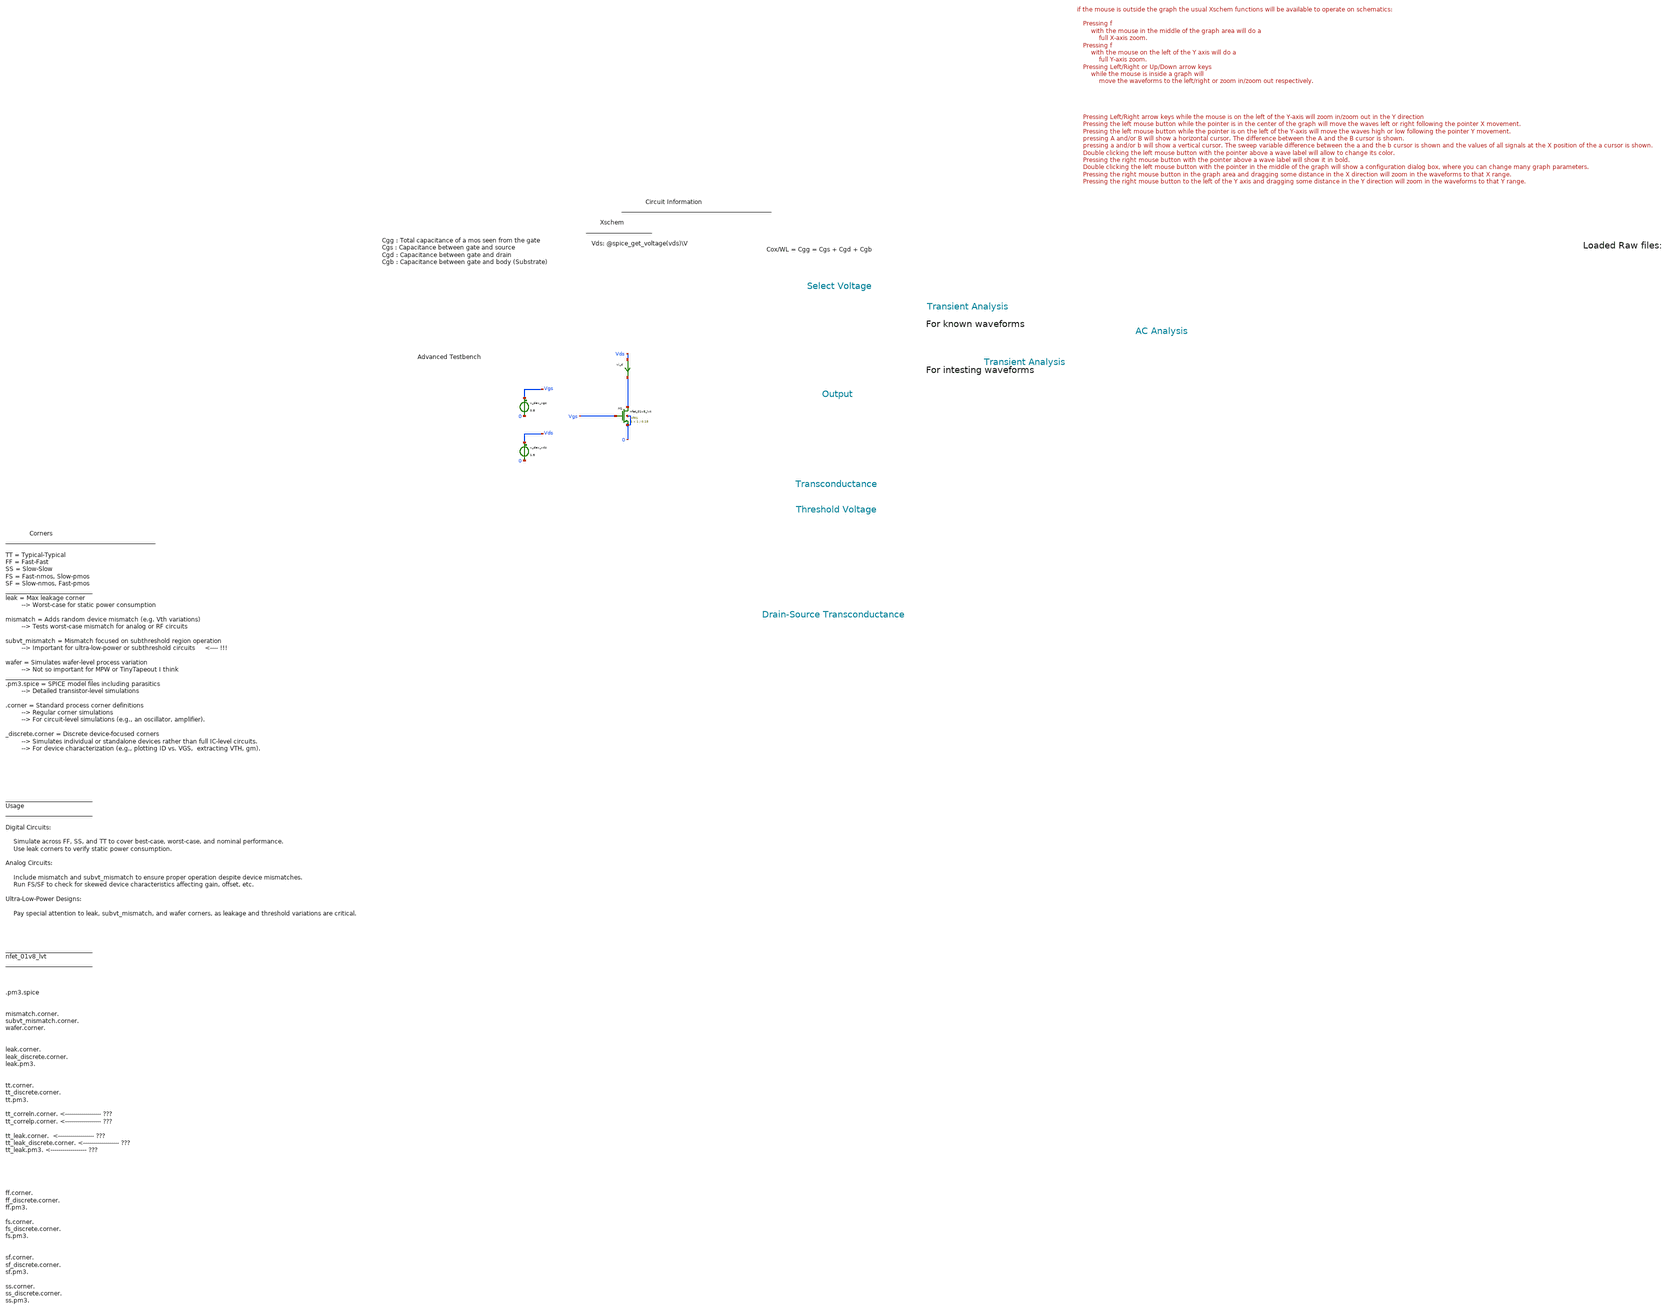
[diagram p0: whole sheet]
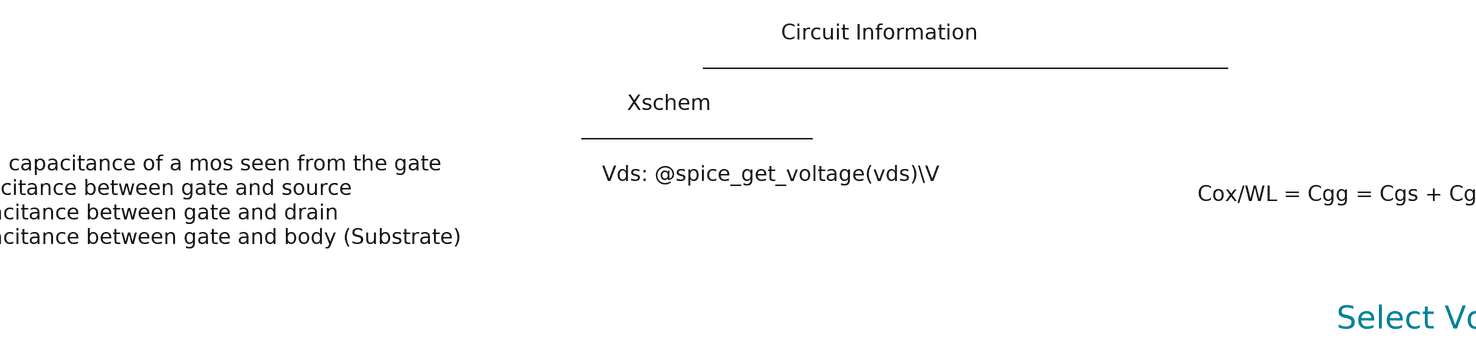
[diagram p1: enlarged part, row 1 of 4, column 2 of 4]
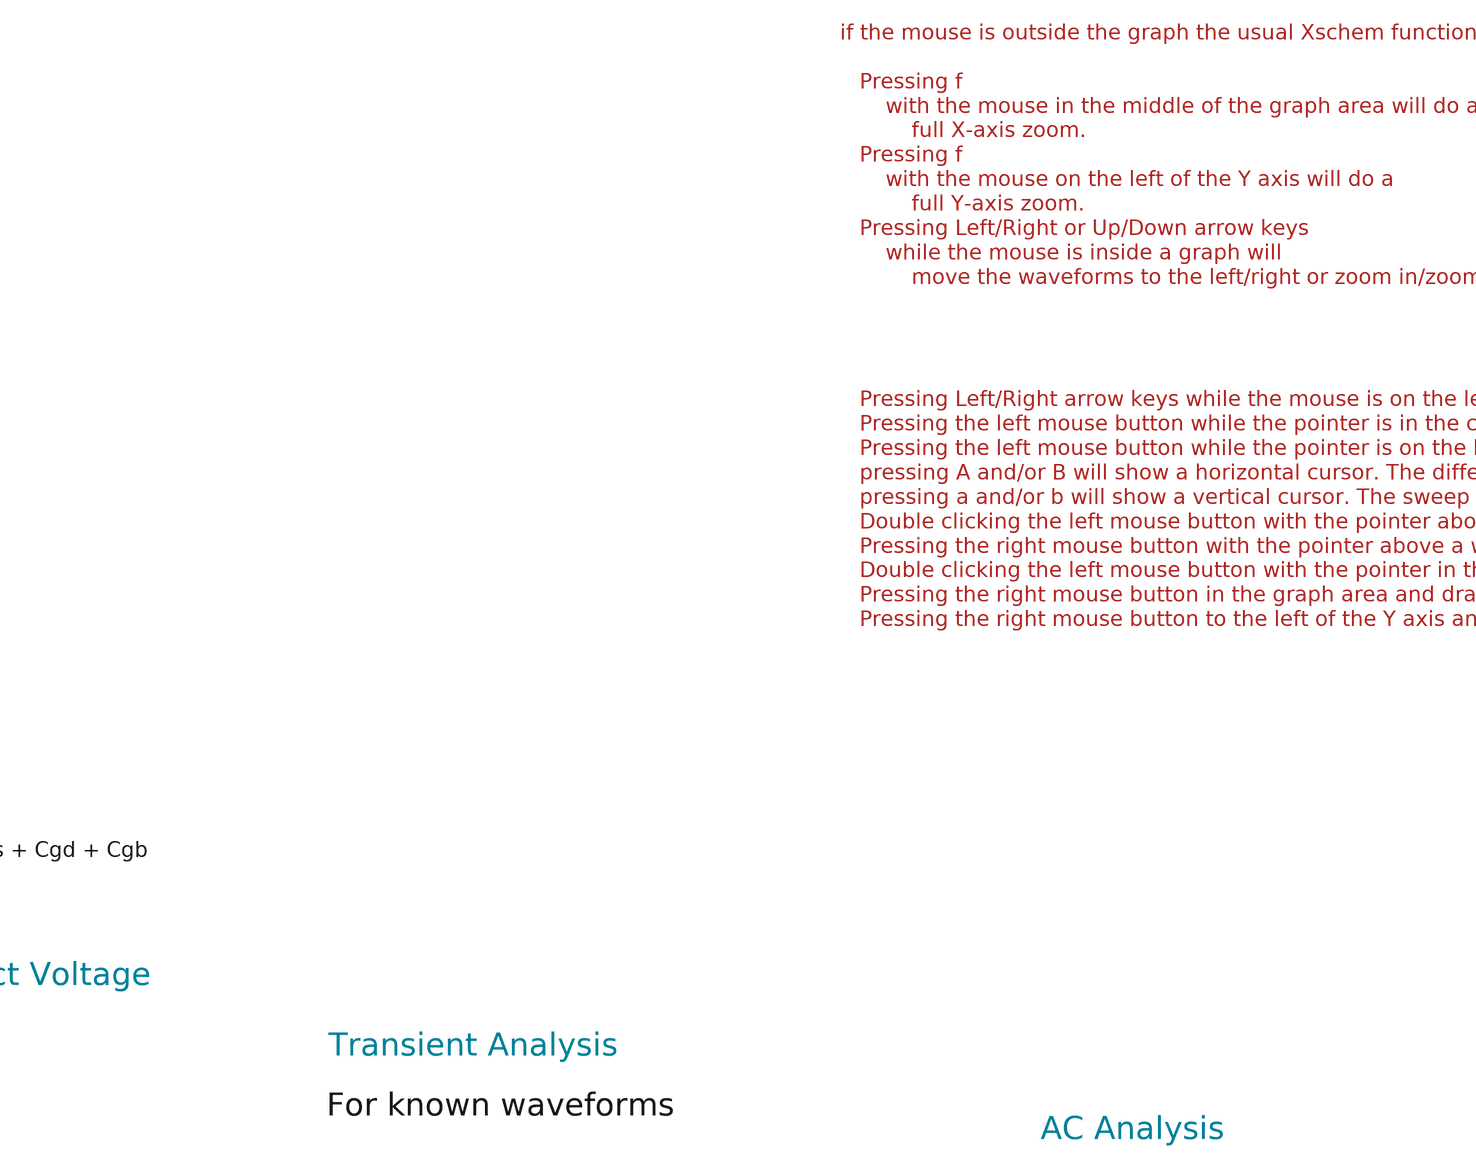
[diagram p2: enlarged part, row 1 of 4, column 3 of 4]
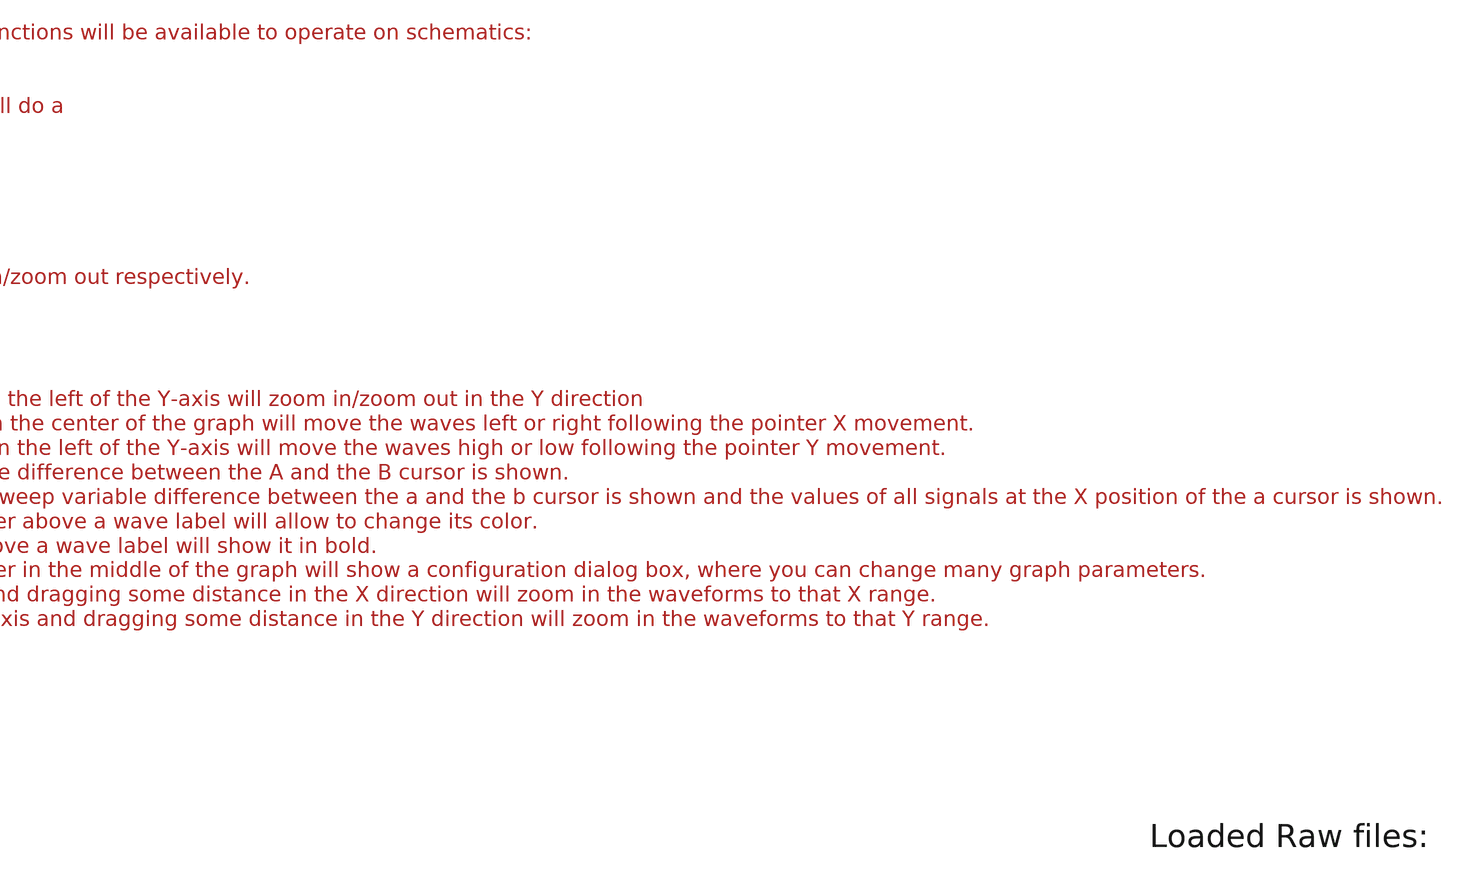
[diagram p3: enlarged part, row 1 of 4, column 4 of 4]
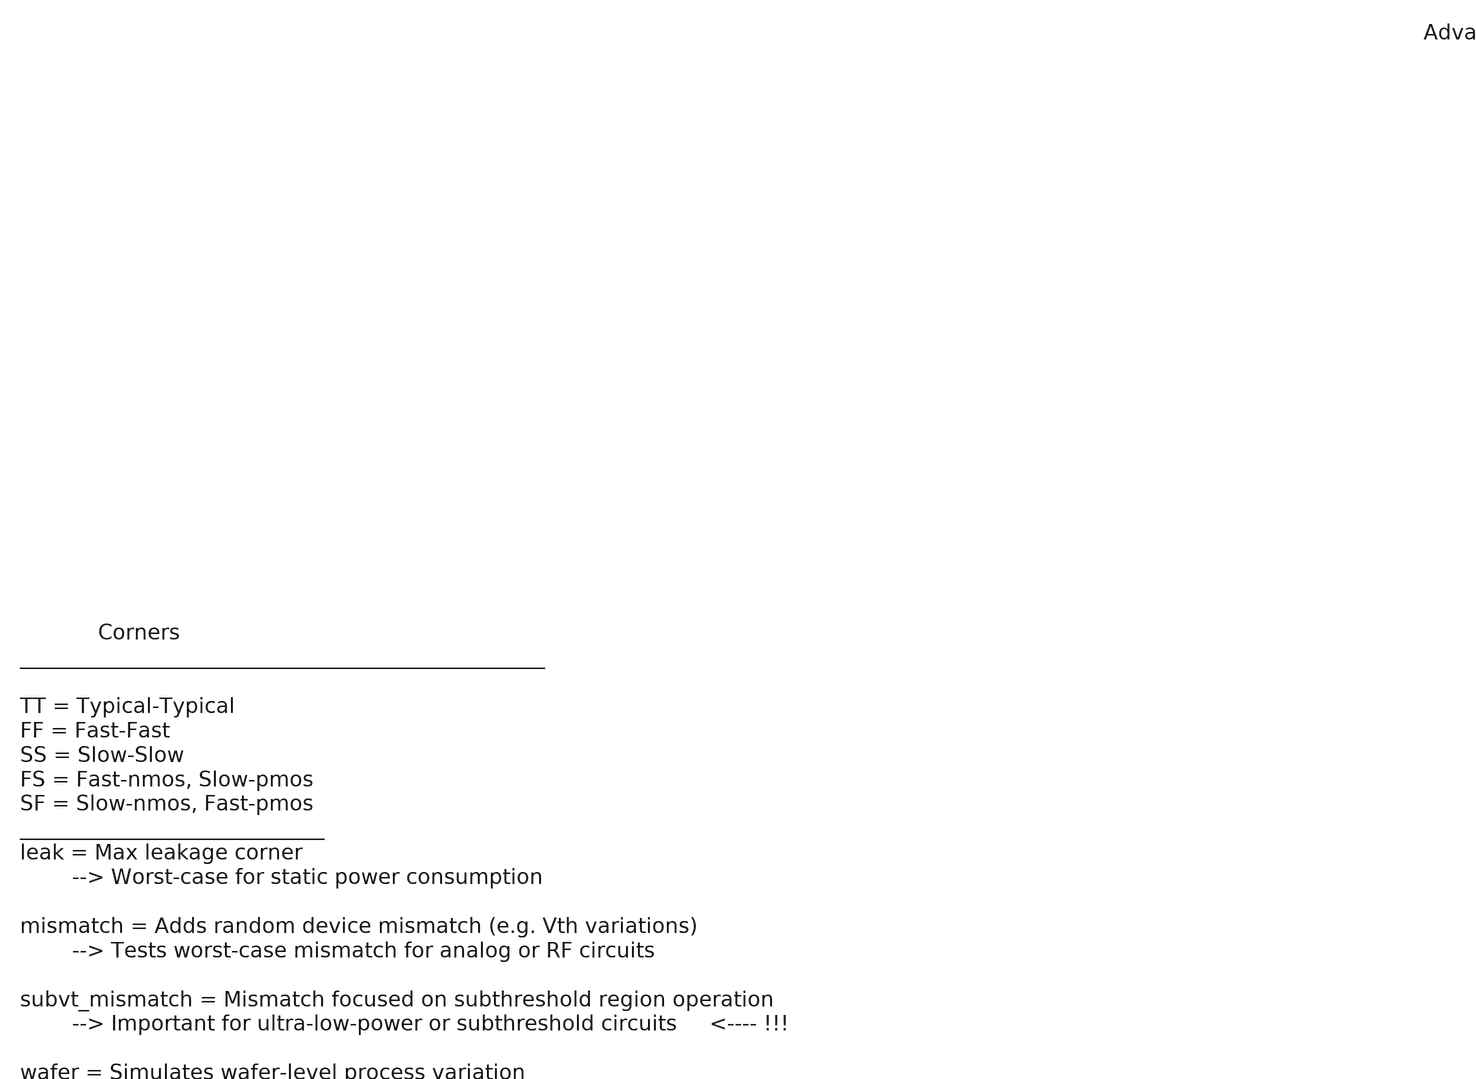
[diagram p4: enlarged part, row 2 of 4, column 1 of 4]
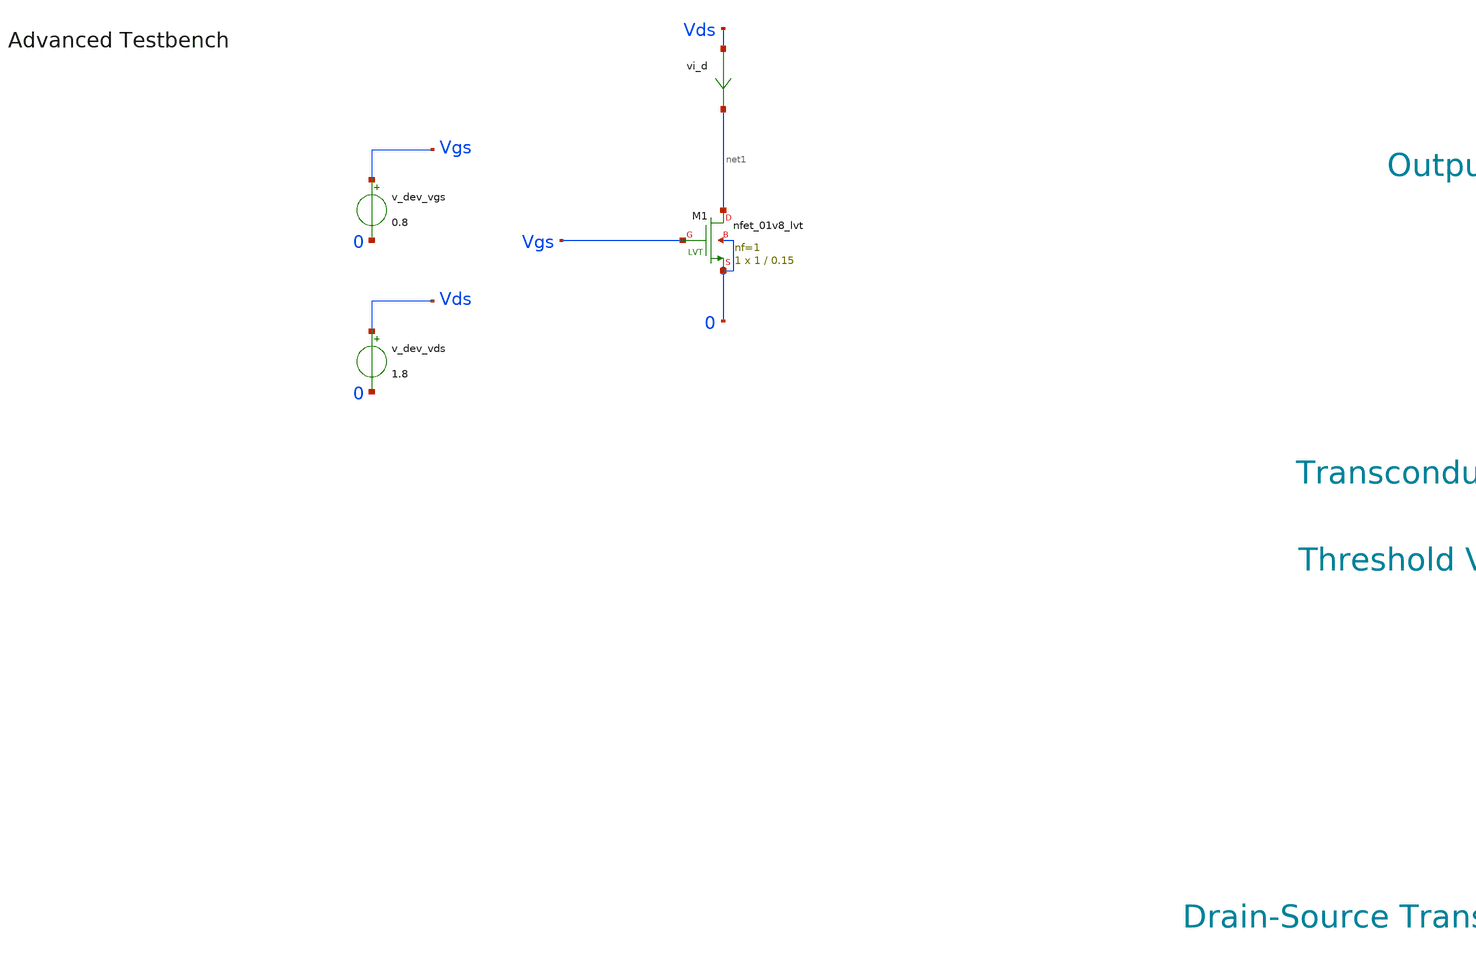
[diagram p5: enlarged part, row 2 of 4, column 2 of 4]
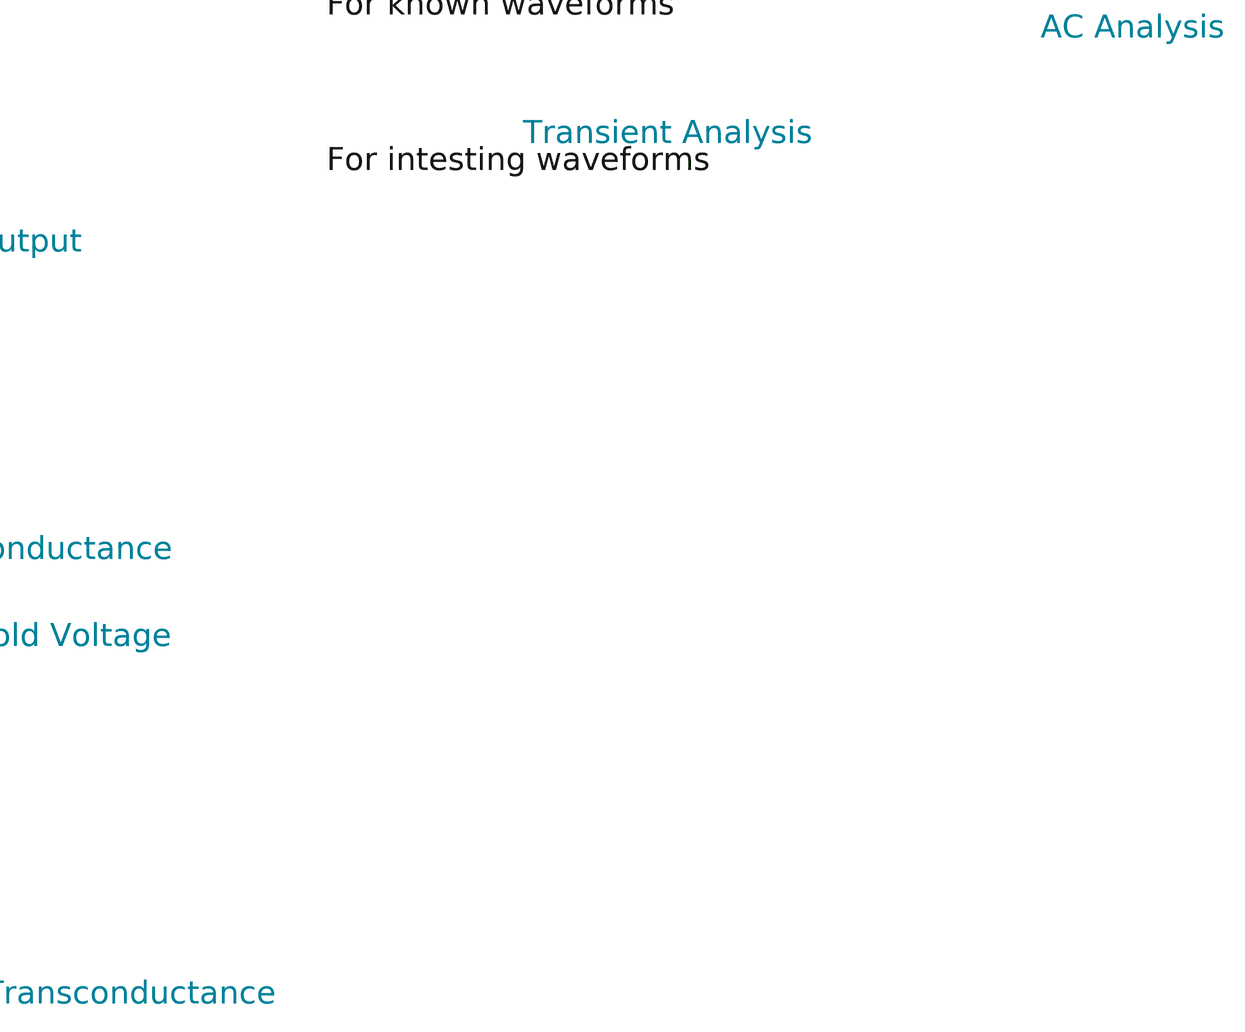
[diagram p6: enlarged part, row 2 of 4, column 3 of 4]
** sch_path: xschem/T0/nmos.sch
* Copyright (C) 1998-2024 Stefan Frederik Schippers
* This program is free software; you can redistribute it and/or modify
* it under the terms of the GNU General Public License as published by
* the Free Software Foundation; either version 2 of the License, or
* (at your option) any later version.
* This program is distributed in the hope that it will be useful,
* but WITHOUT ANY WARRANTY; without even the implied warranty of
* MERCHANTABILITY or FITNESS FOR A PARTICULAR PURPOSE.  See the
* GNU General Public License for more details.
* You should have received a copy of the GNU General Public License
* along with this program; if not, write to the Free Software
**.subckt nmos
XM1 net1 Vgs 0 0 sky130_fd_pr__nfet_01v8_lvt L=0.15 W=1 nf=1 ad='int((1 + 1)/2) * 1 / 1 * 0.29' as='int((1 + 2)/2) * 1 / 1 * 0.29'
+ pd='2*int((1 + 1)/2) * (1 / 1 + 0.29)' ps='2*int((1 + 2)/2) * (1 / 1 + 0.29)' nrd='0.29 / 1 ' nrs='0.29 / 1 '
+ sa=0 sb=0 sd=0 mult=1 m=1
vi_d Vds net1 0
.save i(vi_d)
v_dev_vds Vds 0 1.8
v_dev_vgs Vgs 0 0.8
**** begin user architecture code



.temp 30
*.param w_width = 1
*.param l_length = 0.15
*.option gmin=5n
*.option scale=1e-6
*.option wnflag=1
.option savecurrents

.save all
.control
  save all alli

  save @m.xm1.msky130_fd_pr__nfet_01v8_lvt[gm]
  save @m.xm1.msky130_fd_pr__nfet_01v8_lvt[id]
  save @m.xm1.msky130_fd_pr__nfet_01v8_lvt[vgs]

  save @m.xm1.msky130_fd_pr__nfet_01v8_lvt[cgg]
  save @m.xm1.msky130_fd_pr__nfet_01v8_lvt[cgs]
  save @m.xm1.msky130_fd_pr__nfet_01v8_lvt[cgd]
  save @m.xm1.msky130_fd_pr__nfet_01v8_lvt[cgb]

  save @m.xm1.msky130_fd_pr__nfet_01v8_lvt[vds]
  save @m.xm1.msky130_fd_pr__nfet_01v8_lvt[vdsat]
  save @m.xm1.msky130_fd_pr__nfet_01v8_lvt[vth]


  save @m.xm1.msky130_fd_pr__nfet_01v8_lvt[leff]
  save @m.xm1.msky130_fd_pr__nfet_01v8_lvt[weff]
  save @m.xm1.msky130_fd_pr__nfet_01v8_lvt[gds]
  save @m.xm1.msky130_fd_pr__nfet_01v8_lvt[l]
  save @m.xm1.msky130_fd_pr__nfet_01v8_lvt[w]
  save @m.xm1.msky130_fd_pr__nfet_01v8_lvt[gm]
  save @m.xm1.msky130_fd_pr__nfet_01v8_lvt[gm]
  save @m.xm1.msky130_fd_pr__nfet_01v8_lvt[gm]
  save @m.xm1.msky130_fd_pr__nfet_01v8_lvt[gm]
  save @m.xm1.msky130_fd_pr__nfet_01v8_lvt[gm]


  dc v_dev_vds 0 1.8  0.01
  *dc v_dev_vds 0 20u  10n
  *v_dev_vgs 1 1.8 0.02
  write nmos_tb.raw


  op
  set appendwrite
  write nmos_tb.raw



  *tran 1n 5u
  *write nmos_tb.raw






  *quit 0




.endc





** opencircuitdesign pdks install
.lib $::SKYWATER_MODELS/sky130.lib.spice tt
.include $::SKYWATER_STDCELLS/sky130_fd_sc_hd.spice


**** end user architecture code
**.ends
.end
